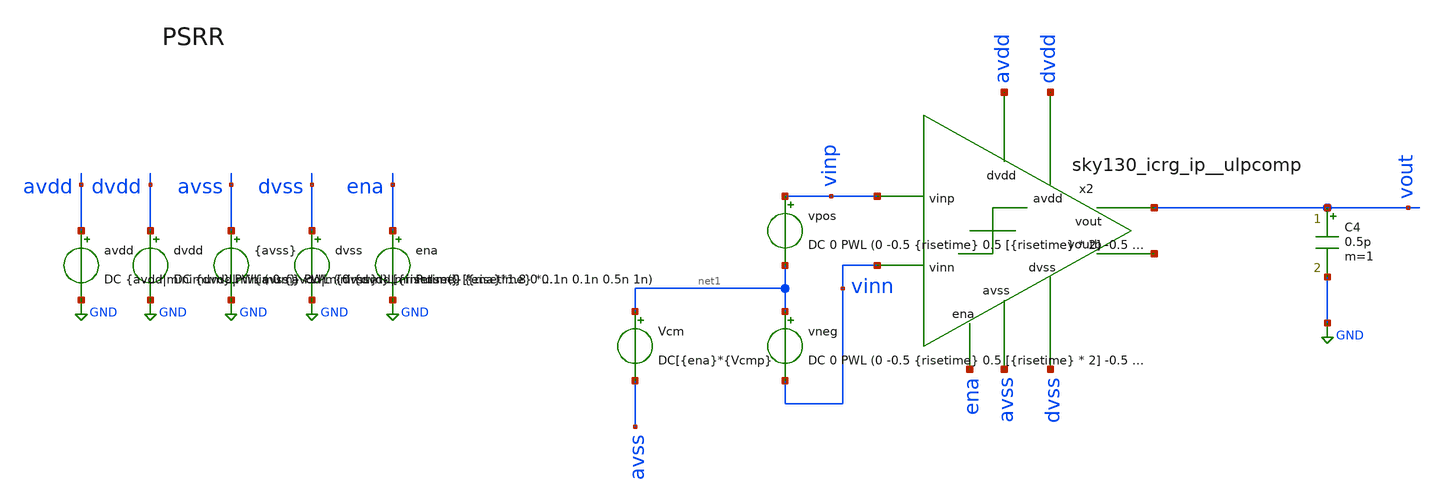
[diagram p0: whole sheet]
** sch_path: cace/tb_PSRR.sch
**.subckt tb_PSRR
x2 avdd dvdd ena vinp vinn vout net2 avss dvss sky130_icrg_ip__ulpcomp
vpos vinp net1 DC 0 PWL (0 -0.5 {risetime} 0.5 [{risetime} * 2] -0.5 [{risetime} * 3] 0.5 [{risetime}
+ * 4] -0.5 )
avdd avdd GND DC {avdd|minimum} PWL ( 0 {avdd|minimum} [{risetime} * 2] {avdd|minimum} [{risetime} *
+ 2 + 1e-9] {avdd|maximum} [{risetime} * 3] {avdd|maximum} )
dvdd dvdd GND DC {dvdd|minimum} PWL ( 0 {dvdd|minimum} [{risetime} * 2] {dvdd|minimum} [{risetime} *
+ 2 + 1e-9] {dvdd|maximum} [{risetime} * 3] {dvdd|maximum} )
{avss} avss GND {avss}
dvss dvss GND {dvss}
C4 vout GND 0.5p m=1
Vcm net1 avss DC[{ena}*{Vcmp}
ena ena GND Pulse(0 {ena}*1.8 0 0.1n 0.1n 0.5n 1n)
vneg net1 vinn DC 0 PWL (0 -0.5 {risetime} 0.5 [{risetime} * 2] -0.5 [{risetime} * 3] 0.5 [{risetime}
+ * 4] -0.5 )
**** begin user architecture code


.lib /home/ttuser/pdk/sky130A/libs.tech/combined/sky130.lib.spice {corner}
.option TEMP={temperature}


.control
** CMRR is defined as the change in input offset vs. change in common-mode voltage.
tran [{risetime} * 2 / 100] [{risetime} * 4]
meas tran vhigh1 FIND V(vinp) WHEN V(vout) = [{dvdd|minimum} / 2] CROSS=1
meas tran vlow1 FIND V(vinp) WHEN V(vout) = [{dvdd|minimum} / 2] CROSS=2
meas tran vhigh2 FIND V(vinp) WHEN V(vout) = [{dvdd|maximum} / 2] CROSS=3
meas tran vlow2 FIND V(vinp) WHEN V(vout) = [{dvdd|maximum} / 2] CROSS=4

let voffset1 = 0.5 * ($&vhigh1 + $&vlow1)
let voffset2 = 0.5 * ($&vhigh2 + $&vlow2)

let psrr = ($&voffset1 - $&voffset2) / ({dvdd|maximum} - {dvdd|minimum})
let psrrdb = 20 * log(abs($&psrr))

echo $&cmrrdb > {simpath}/{filename}_{N}.data
quit
.endc


**** end user architecture code
**.ends
.GLOBAL GND
.end
